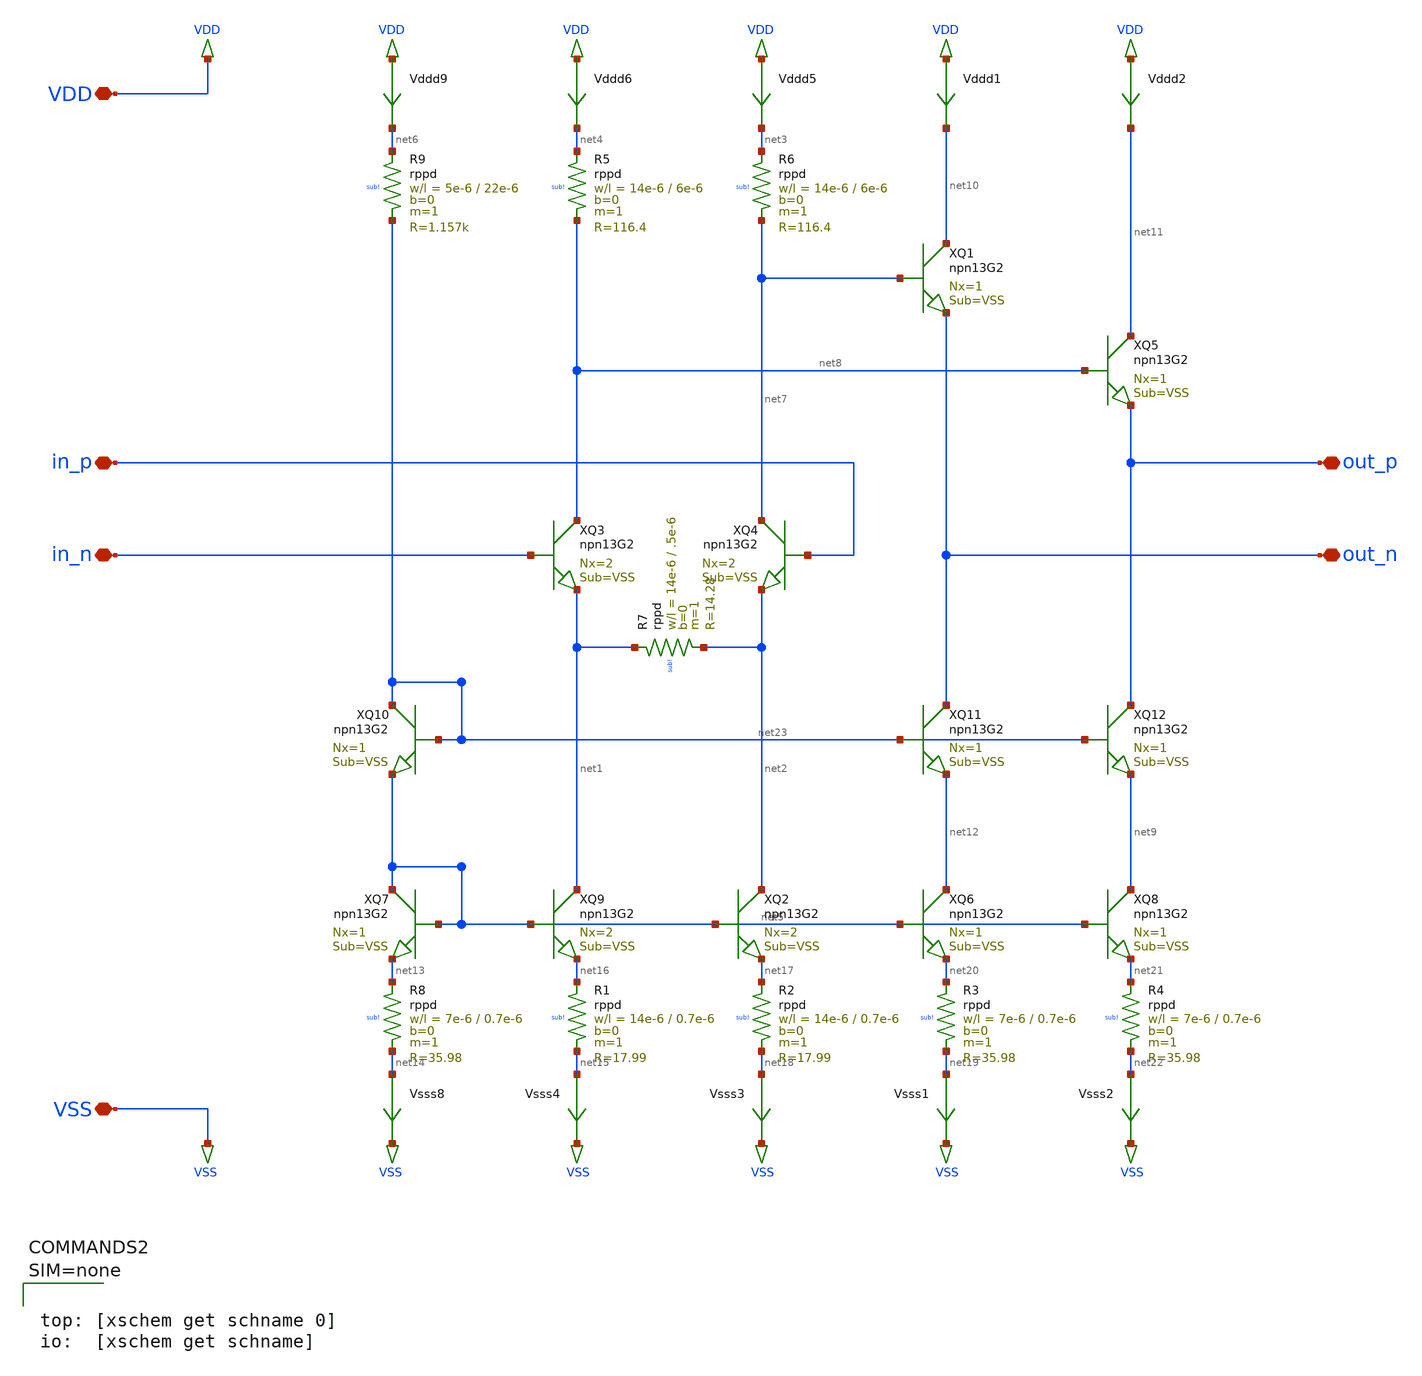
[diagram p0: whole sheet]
** sch_path: HBT_VCO_active_L/design_data/xschem/AMP_DiFF_100R.sch
* Copyright (C) 1998-2023 Stefan Frederik Schippers
* This program is free software; you can redistribute it and/or modify
* it under the terms of the GNU General Public License as published by
* the Free Software Foundation; either version 2 of the License, or
* (at your option) any later version.
* This program is distributed in the hope that it will be useful,
* but WITHOUT ANY WARRANTY; without even the implied warranty of
* MERCHANTABILITY or FITNESS FOR A PARTICULAR PURPOSE.  See the
* GNU General Public License for more details.
* You should have received a copy of the GNU General Public License
* along with this program; if not, write to the Free Software
**.subckt AMP_DiFF_100R VSS VDD out_p out_n in_p in_n
*.iopin VSS
*.iopin VDD
*.iopin out_p
*.iopin out_n
*.iopin in_p
*.iopin in_n
Vsss3 net18 VSS 0
.save i(vsss3)
XQ2 net2 net5 net17 VSS npn13G2 Nx=2
XQ3 net8 in_n net1 VSS npn13G2 Nx=2
XQ4 net7 in_p net2 VSS npn13G2 Nx=2
Vddd5 VDD net3 0
.save i(vddd5)
Vddd6 VDD net4 0
.save i(vddd6)
Vsss8 net14 VSS 0
.save i(vsss8)
XQ7 net5 net5 net13 VSS npn13G2 Nx=1
Vddd9 VDD net6 0
.save i(vddd9)
XQ1 net10 net7 out_n VSS npn13G2 Nx=1
XQ5 net11 net8 out_p VSS npn13G2 Nx=1
Vddd1 VDD net10 0
.save i(vddd1)
Vddd2 VDD net11 0
.save i(vddd2)
Vsss1 net19 VSS 0
.save i(vsss1)
XQ6 net12 net5 net20 VSS npn13G2 Nx=1
Vsss2 net22 VSS 0
.save i(vsss2)
XQ8 net9 net5 net21 VSS npn13G2 Nx=1
Vsss4 net15 VSS 0
.save i(vsss4)
XQ9 net1 net5 net16 VSS npn13G2 Nx=2
XR8 net13 net14 sub! rppd w=7e-6 l=0.7e-6 m=1 b=0 mm_ok=1
XR1 net16 net15 sub! rppd w=14e-6 l=0.7e-6 m=1 b=0 mm_ok=1
XR2 net17 net18 sub! rppd w=14e-6 l=0.7e-6 m=1 b=0 mm_ok=1
XR3 net20 net19 sub! rppd w=7e-6 l=0.7e-6 m=1 b=0 mm_ok=1
XR4 net21 net22 sub! rppd w=7e-6 l=0.7e-6 m=1 b=0 mm_ok=1
XR5 net4 net8 sub! rppd w=14e-6 l=6e-6 m=1 b=0 mm_ok=1
XR6 net3 net7 sub! rppd w=14e-6 l=6e-6 m=1 b=0 mm_ok=1
XR7 net1 net2 sub! rppd w=14e-6 l=.5e-6 m=1 b=0 mm_ok=1
XR9 net6 net23 sub! rppd w=5e-6 l=22e-6 m=1 b=0 mm_ok=1
XQ10 net23 net23 net5 VSS npn13G2 Nx=1
XQ11 out_n net23 net12 VSS npn13G2 Nx=1
XQ12 out_p net23 net9 VSS npn13G2 Nx=1
**** begin user architecture code



**** end user architecture code
**.ends
.end
